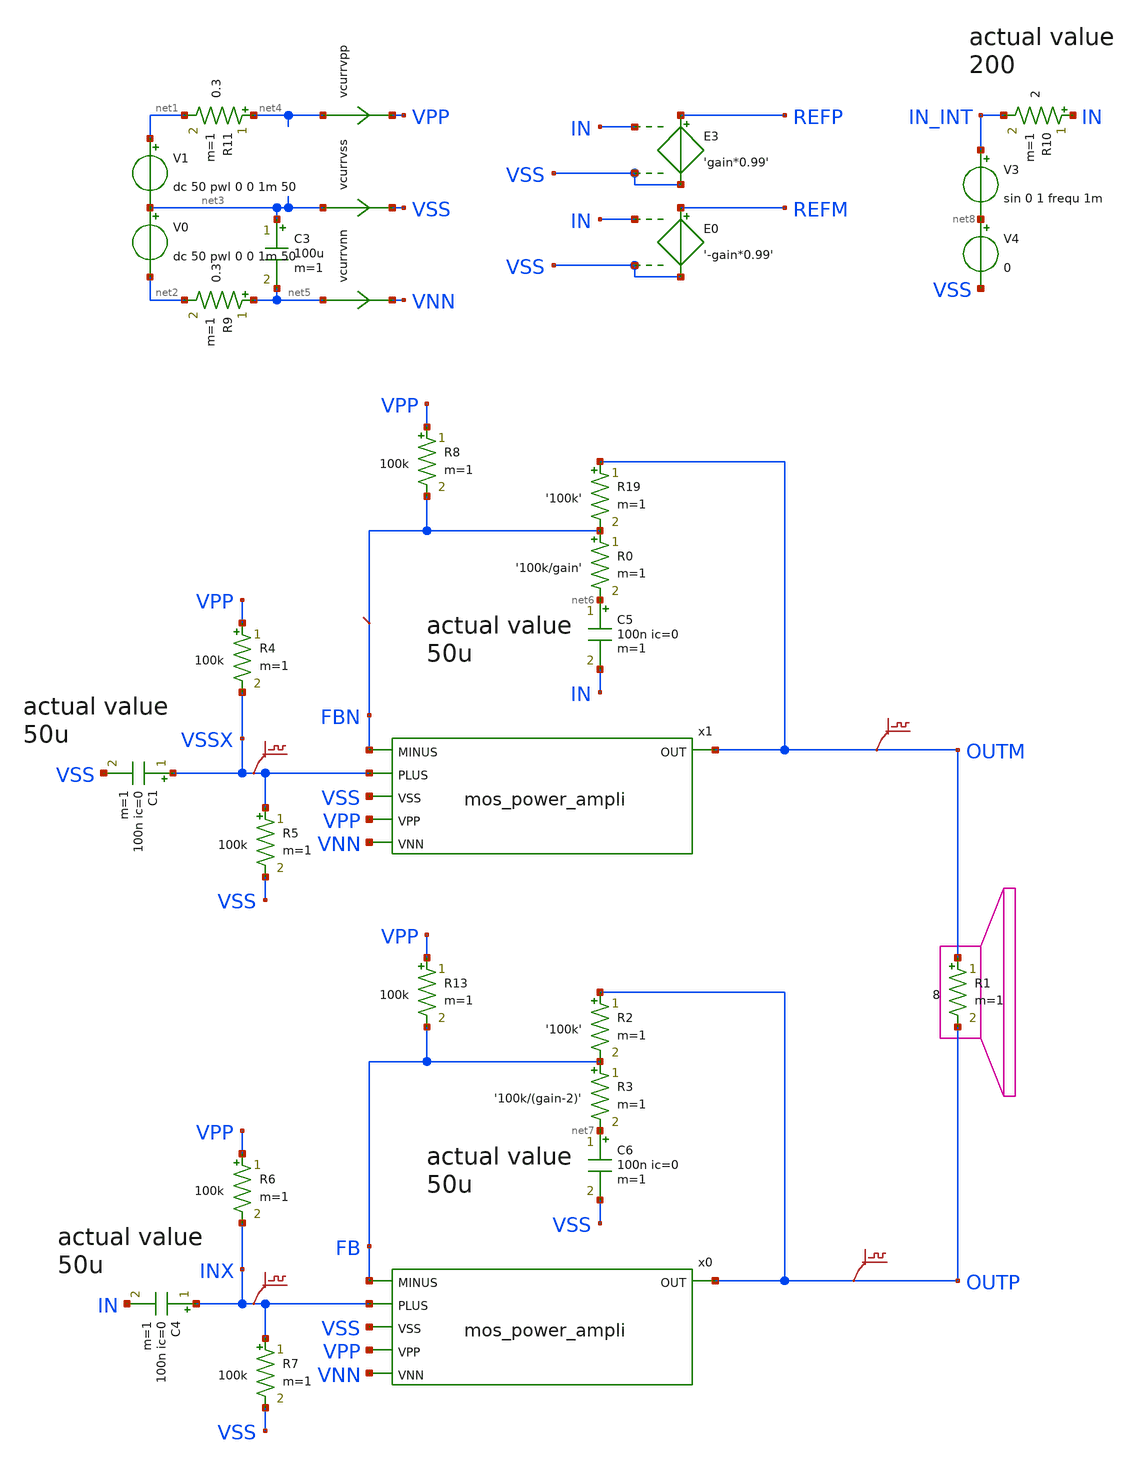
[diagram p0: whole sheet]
** sch_path: xschem_library/examples/poweramp.sch
**.subckt poweramp
V1 net1 net3 dc 50 pwl 0 0 1m 50
V0 net3 net2 dc 50 pwl 0 0 1m 50
R1 OUTM OUTP 8 m=1
E3 REFP VSS IN VSS 'gain*0.99'
C3 net3 net5 100u m=1
R11 net4 net1 0.3 m=1
R9 net5 net2 0.3 m=1
R19 OUTM FBN '100k' m=1
R0 FBN net6 '100k/gain' m=1
x1 FBN VSSX VSS OUTM VPP VNN mos_power_ampli
x0 FB INX VSS OUTP VPP VNN mos_power_ampli
R6 VPP INX 100k m=1
R7 INX VSS 100k m=1
E0 REFM VSS IN VSS '-gain*0.99'
C5 net6 IN 100n ic=0 m=1
C6 net7 VSS 100n ic=0 m=1
R2 OUTP FB '100k' m=1
R3 FB net7 '100k/(gain-2)' m=1
V3 IN_INT net8 sin 0 1 frequ 1m
R4 VPP VSSX 100k m=1
R5 VSSX VSS 100k m=1
R8 VPP FBN 100k m=1
C4 INX IN 100n ic=0 m=1
C1 VSSX VSS 100n ic=0 m=1
R10 IN IN_INT 2 m=1
R13 VPP FB 100k m=1
V4 net8 VSS 0
vcurrvpp net4 VPP 0
.save i(vcurrvpp)
.save v(outm)
.save v(outp)
vcurrvnn net5 VNN 0
.save i(vcurrvnn)
vcurrvss net3 VSS 0
.save i(vcurrvss)
.save v(inx)
.save v(vssx)
**** begin user architecture code

.option PARHIER=LOCAL RUNLVL=6 post MODMONTE=1 warn maxwarns=400
.option ITL4=20000 ITL5=0
* .option sampling_method = SRS
* .option method=gear
vvss vss 0 dc 0
.temp 30

.param frequ=20k
.param gain=42
.op
.tran  6e-7 0.009 uic


** models are generally not free: you must download
** SPICE models for active devices and put them  into the below
** referenced file in simulation directory.
.include "models_poweramp.txt"
.save all
.option savecurrents
* .FOUR 20k v(outm,outp)
* .probe i(*)
* .probe p(r*) p(v*)


**** end user architecture code
**.ends

* expanding   symbol:  mos_power_ampli.sym # of pins=6
** sym_path: xschem_library/examples/mos_power_ampli.sym
** sch_path: xschem_library/examples/mos_power_ampli.sch
.subckt mos_power_ampli MINUS PLUS VSS OUT VPP VNN
*.ipin PLUS
*.ipin VPP
*.ipin VNN
*.opin OUT
*.ipin MINUS
*.ipin VSS
xm2 net2 GB SB irf540 m=1
R7 GB SB 190 m=1
xm1 VPP GA SA irf540 m=1
R0 GA SA 190 m=1
R2 VPP E2 50 m=1
R3 VBOOST E1 50 m=1
Q5 C5 PLUS E9 q2n2222 area=1 m=1
Q4 net9 net3 E4 q2n2907p area=1 m=1
R9 VBOOST E4 50 m=1
Q6 C6 C2 net6 q2n2907p area=1 m=1
R4 VPP E6 50 m=1
vd net1 net2 0
.save i(vd)
vu SA net1 0
.save i(vu)
Q1 net3 net3 E1 q2n2907p area=1 m=1
Q2 C2 C2 net5 q2n2907p area=1 m=1
Q9 C9 MINUS E9 q2n2222 area=1 m=1
R11 GB net7 1300 m=1
Q8 C8 VSS E8 q2n2907p area=1 m=1
C12 VBOOST net4 40u m=1
D0 VPP VBOOST d1n4148 area=1
R18 net4 net1 200 m=1
D1 VPP VBOOST d1n758
R14 B1 net8 4k m=1
Q11 GA B1 E11 q2n2907p area=1 m=1
R15 VBOOST B1 4k m=1
R5 E9 net10 600 m=1
R6 net10 net11 700 m=1
D2 VNN B3 d1n755
Q3 C3 B3 E3 q2n2222 area=1 m=1
R1 VSS B3 10k m=1
R10 E3 VNN 170 m=1
C3 B3 VNN 100n m=1
R12 C6 E8 1300 m=1
R13 C2 C9 300 m=1
Q7 C7 C9 C5 q2n2222 area=1 m=1
v0 SB VNN 0
.save i(v0)
v1 E6 net6 0
.save i(v1)
v2 E2 net5 0
.save i(v2)
v3 net11 C3 0
.save i(v3)
v4 C8 net7 0
.save i(v4)
v5 net8 net1 0
.save i(v5)
v6 net3 C7 0
.save i(v6)
v7 net9 E11 0
.save i(v7)
.save v(gb)
.save v(gb)
.save v(sb)
.save v(ga)
.save v(sa)
.save v(ga)
.save v(net1)
.save v(minus)
.save v(plus)
.save v(e9)
.save v(c2)
.save v(net3)
.save v(b1)
v8 net1 OUT 0
.save i(v8)
.save v(c9)
.save v(net5)
.save v(b3)
.save v(vpp)
.save v(vnn)
**** begin user architecture code

* .probe v(ga,sa) v(gb,sb)
* .probe p(q*) p(r*) i(r*) p(xm1) p(xm2) i(d*)
**** end user architecture code
.ends

.end
